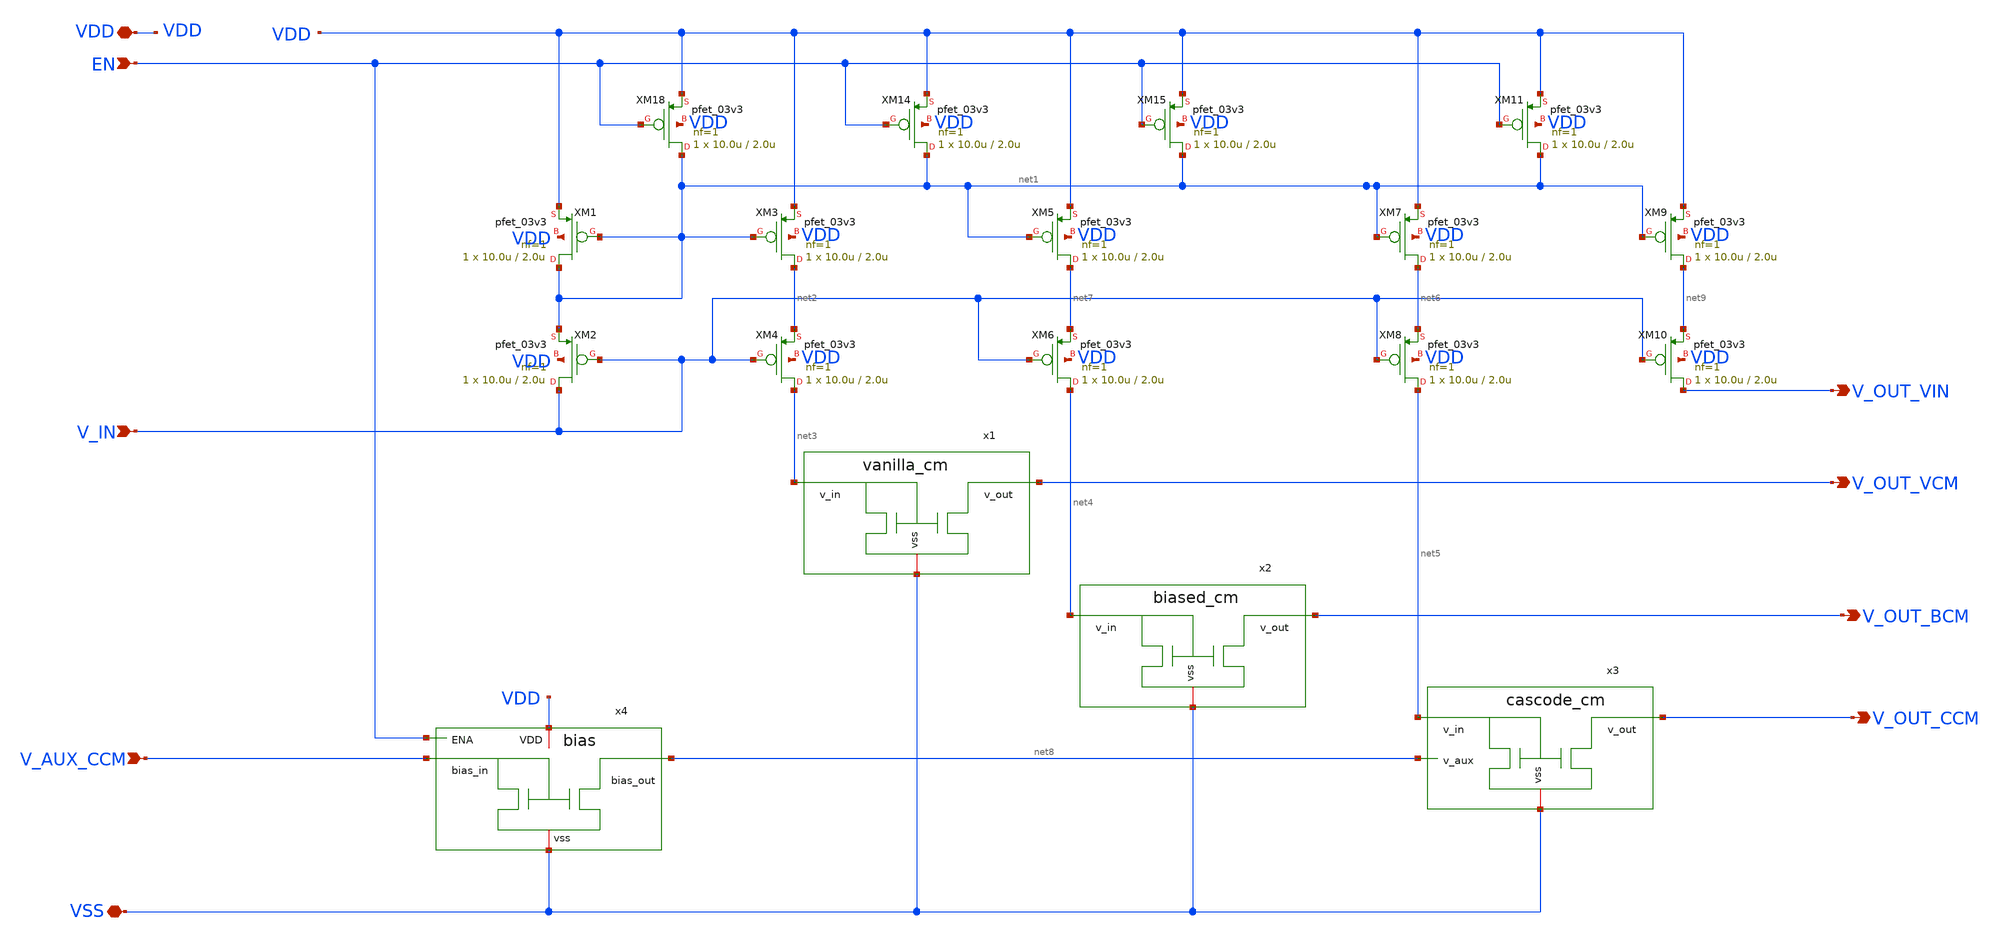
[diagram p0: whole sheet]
** sch_path: blocks/composite/regulated_cascoded_cmirror/xschem/top_level.sch
**.subckt top_level VSS V_AUX_CCM VDD V_OUT_VCM V_OUT_BCM V_OUT_CCM V_IN EN V_OUT_VIN
*.iopin VSS
*.ipin V_AUX_CCM
*.iopin VDD
*.opin V_OUT_VCM
*.opin V_OUT_BCM
*.opin V_OUT_CCM
*.ipin V_IN
*.ipin EN
*.opin V_OUT_VIN
XM1 net1 net1 VDD VDD pfet_03v3 L=2.0u W=10.0u nf=1 ad='int((nf+1)/2) * W/nf * 0.18u' as='int((nf+2)/2) * W/nf * 0.18u'
+ pd='2*int((nf+1)/2) * (W/nf + 0.18u)' ps='2*int((nf+2)/2) * (W/nf + 0.18u)' nrd='0.18u / W' nrs='0.18u / W'
+ sa=0 sb=0 sd=0 m=1
XM2 V_IN V_IN net1 VDD pfet_03v3 L=2.0u W=10.0u nf=1 ad='int((nf+1)/2) * W/nf * 0.18u' as='int((nf+2)/2) * W/nf * 0.18u'
+ pd='2*int((nf+1)/2) * (W/nf + 0.18u)' ps='2*int((nf+2)/2) * (W/nf + 0.18u)' nrd='0.18u / W' nrs='0.18u / W'
+ sa=0 sb=0 sd=0 m=1
XM3 net2 net1 VDD VDD pfet_03v3 L=2.0u W=10.0u nf=1 ad='int((nf+1)/2) * W/nf * 0.18u' as='int((nf+2)/2) * W/nf * 0.18u'
+ pd='2*int((nf+1)/2) * (W/nf + 0.18u)' ps='2*int((nf+2)/2) * (W/nf + 0.18u)' nrd='0.18u / W' nrs='0.18u / W'
+ sa=0 sb=0 sd=0 m=1
XM4 net3 V_IN net2 VDD pfet_03v3 L=2.0u W=10.0u nf=1 ad='int((nf+1)/2) * W/nf * 0.18u' as='int((nf+2)/2) * W/nf * 0.18u'
+ pd='2*int((nf+1)/2) * (W/nf + 0.18u)' ps='2*int((nf+2)/2) * (W/nf + 0.18u)' nrd='0.18u / W' nrs='0.18u / W'
+ sa=0 sb=0 sd=0 m=1
XM5 net7 net1 VDD VDD pfet_03v3 L=2.0u W=10.0u nf=1 ad='int((nf+1)/2) * W/nf * 0.18u' as='int((nf+2)/2) * W/nf * 0.18u'
+ pd='2*int((nf+1)/2) * (W/nf + 0.18u)' ps='2*int((nf+2)/2) * (W/nf + 0.18u)' nrd='0.18u / W' nrs='0.18u / W'
+ sa=0 sb=0 sd=0 m=1
XM6 net4 V_IN net7 VDD pfet_03v3 L=2.0u W=10.0u nf=1 ad='int((nf+1)/2) * W/nf * 0.18u' as='int((nf+2)/2) * W/nf * 0.18u'
+ pd='2*int((nf+1)/2) * (W/nf + 0.18u)' ps='2*int((nf+2)/2) * (W/nf + 0.18u)' nrd='0.18u / W' nrs='0.18u / W'
+ sa=0 sb=0 sd=0 m=1
XM7 net6 net1 VDD VDD pfet_03v3 L=2.0u W=10.0u nf=1 ad='int((nf+1)/2) * W/nf * 0.18u' as='int((nf+2)/2) * W/nf * 0.18u'
+ pd='2*int((nf+1)/2) * (W/nf + 0.18u)' ps='2*int((nf+2)/2) * (W/nf + 0.18u)' nrd='0.18u / W' nrs='0.18u / W'
+ sa=0 sb=0 sd=0 m=1
XM8 net5 V_IN net6 VDD pfet_03v3 L=2.0u W=10.0u nf=1 ad='int((nf+1)/2) * W/nf * 0.18u' as='int((nf+2)/2) * W/nf * 0.18u'
+ pd='2*int((nf+1)/2) * (W/nf + 0.18u)' ps='2*int((nf+2)/2) * (W/nf + 0.18u)' nrd='0.18u / W' nrs='0.18u / W'
+ sa=0 sb=0 sd=0 m=1
XM14 net1 EN VDD VDD pfet_03v3 L=2.0u W=10.0u nf=1 ad='int((nf+1)/2) * W/nf * 0.18u' as='int((nf+2)/2) * W/nf * 0.18u'
+ pd='2*int((nf+1)/2) * (W/nf + 0.18u)' ps='2*int((nf+2)/2) * (W/nf + 0.18u)' nrd='0.18u / W' nrs='0.18u / W'
+ sa=0 sb=0 sd=0 m=1
XM18 net1 EN VDD VDD pfet_03v3 L=2.0u W=10.0u nf=1 ad='int((nf+1)/2) * W/nf * 0.18u' as='int((nf+2)/2) * W/nf * 0.18u'
+ pd='2*int((nf+1)/2) * (W/nf + 0.18u)' ps='2*int((nf+2)/2) * (W/nf + 0.18u)' nrd='0.18u / W' nrs='0.18u / W'
+ sa=0 sb=0 sd=0 m=1
XM15 net1 EN VDD VDD pfet_03v3 L=2.0u W=10.0u nf=1 ad='int((nf+1)/2) * W/nf * 0.18u' as='int((nf+2)/2) * W/nf * 0.18u'
+ pd='2*int((nf+1)/2) * (W/nf + 0.18u)' ps='2*int((nf+2)/2) * (W/nf + 0.18u)' nrd='0.18u / W' nrs='0.18u / W'
+ sa=0 sb=0 sd=0 m=1
x1 net3 V_OUT_VCM VSS vanilla_cm
x2 V_OUT_BCM net4 VSS biased_cm
x3 V_OUT_CCM net8 net5 VSS cascode_cm
x4 VDD EN V_AUX_CCM net8 VSS bias
XM9 net9 net1 VDD VDD pfet_03v3 L=2.0u W=10.0u nf=1 ad='int((nf+1)/2) * W/nf * 0.18u' as='int((nf+2)/2) * W/nf * 0.18u'
+ pd='2*int((nf+1)/2) * (W/nf + 0.18u)' ps='2*int((nf+2)/2) * (W/nf + 0.18u)' nrd='0.18u / W' nrs='0.18u / W'
+ sa=0 sb=0 sd=0 m=1
XM10 V_OUT_VIN V_IN net9 VDD pfet_03v3 L=2.0u W=10.0u nf=1 ad='int((nf+1)/2) * W/nf * 0.18u' as='int((nf+2)/2) * W/nf * 0.18u'
+ pd='2*int((nf+1)/2) * (W/nf + 0.18u)' ps='2*int((nf+2)/2) * (W/nf + 0.18u)' nrd='0.18u / W' nrs='0.18u / W'
+ sa=0 sb=0 sd=0 m=1
XM11 net1 EN VDD VDD pfet_03v3 L=2.0u W=10.0u nf=1 ad='int((nf+1)/2) * W/nf * 0.18u' as='int((nf+2)/2) * W/nf * 0.18u'
+ pd='2*int((nf+1)/2) * (W/nf + 0.18u)' ps='2*int((nf+2)/2) * (W/nf + 0.18u)' nrd='0.18u / W' nrs='0.18u / W'
+ sa=0 sb=0 sd=0 m=1
**.ends

* expanding   symbol:  vanilla_cm.sym # of pins=3
** sym_path: vanilla_cm.sym
** sch_path: vanilla_cm.sch
.subckt vanilla_cm v_in v_out vss
*.ipin v_in
*.iopin vss
*.opin v_out
XM1 v_out v_in vss vss nfet_03v3 L=1u W=4u nf=1 ad='int((nf+1)/2) * W/nf * 0.18u' as='int((nf+2)/2) * W/nf * 0.18u'
+ pd='2*int((nf+1)/2) * (W/nf + 0.18u)' ps='2*int((nf+2)/2) * (W/nf + 0.18u)' nrd='0.18u / W' nrs='0.18u / W'
+ sa=0 sb=0 sd=0 m=1
XM2 v_in v_in vss vss nfet_03v3 L=1u W=4u nf=1 ad='int((nf+1)/2) * W/nf * 0.18u' as='int((nf+2)/2) * W/nf * 0.18u'
+ pd='2*int((nf+1)/2) * (W/nf + 0.18u)' ps='2*int((nf+2)/2) * (W/nf + 0.18u)' nrd='0.18u / W' nrs='0.18u / W'
+ sa=0 sb=0 sd=0 m=1
.ends


* expanding   symbol:  biased_cm.sym # of pins=3
** sym_path: biased_cm.sym
** sch_path: biased_cm.sch
.subckt biased_cm v_out v_in vss
*.ipin v_in
*.iopin vss
*.opin v_out
XM3 net2 net1 vss vss nfet_03v3 L=1u W=4u nf=1 ad='int((nf+1)/2) * W/nf * 0.18u' as='int((nf+2)/2) * W/nf * 0.18u'
+ pd='2*int((nf+1)/2) * (W/nf + 0.18u)' ps='2*int((nf+2)/2) * (W/nf + 0.18u)' nrd='0.18u / W' nrs='0.18u / W'
+ sa=0 sb=0 sd=0 m=1
XM4 net1 net1 vss vss nfet_03v3 L=1u W=4u nf=1 ad='int((nf+1)/2) * W/nf * 0.18u' as='int((nf+2)/2) * W/nf * 0.18u'
+ pd='2*int((nf+1)/2) * (W/nf + 0.18u)' ps='2*int((nf+2)/2) * (W/nf + 0.18u)' nrd='0.18u / W' nrs='0.18u / W'
+ sa=0 sb=0 sd=0 m=1
XM5 v_out v_in net2 vss nfet_03v3 L=1u W=4u nf=1 ad='int((nf+1)/2) * W/nf * 0.18u' as='int((nf+2)/2) * W/nf * 0.18u'
+ pd='2*int((nf+1)/2) * (W/nf + 0.18u)' ps='2*int((nf+2)/2) * (W/nf + 0.18u)' nrd='0.18u / W' nrs='0.18u / W'
+ sa=0 sb=0 sd=0 m=1
XM6 v_in v_in net1 vss nfet_03v3 L=1u W=4u nf=1 ad='int((nf+1)/2) * W/nf * 0.18u' as='int((nf+2)/2) * W/nf * 0.18u'
+ pd='2*int((nf+1)/2) * (W/nf + 0.18u)' ps='2*int((nf+2)/2) * (W/nf + 0.18u)' nrd='0.18u / W' nrs='0.18u / W'
+ sa=0 sb=0 sd=0 m=1
.ends


* expanding   symbol:  cascode_cm.sym # of pins=4
** sym_path: cascode_cm.sym
** sch_path: cascode_cm.sch
.subckt cascode_cm v_out v_aux v_in vss
*.ipin v_in
*.iopin vss
*.ipin v_aux
*.opin v_out
XM10 v_aux net1 vss vss nfet_03v3 L=1u W=5u nf=1 ad='int((nf+1)/2) * W/nf * 0.18u' as='int((nf+2)/2) * W/nf * 0.18u'
+ pd='2*int((nf+1)/2) * (W/nf + 0.18u)' ps='2*int((nf+2)/2) * (W/nf + 0.18u)' nrd='0.18u / W' nrs='0.18u / W'
+ sa=0 sb=0 sd=0 m=1
XM8 v_in v_aux net1 vss nfet_03v3 L=1u W=5u nf=1 ad='int((nf+1)/2) * W/nf * 0.18u' as='int((nf+2)/2) * W/nf * 0.18u'
+ pd='2*int((nf+1)/2) * (W/nf + 0.18u)' ps='2*int((nf+2)/2) * (W/nf + 0.18u)' nrd='0.18u / W' nrs='0.18u / W'
+ sa=0 sb=0 sd=0 m=1
XM11 net1 v_in vss vss nfet_03v3 L=1u W=5u nf=1 ad='int((nf+1)/2) * W/nf * 0.18u' as='int((nf+2)/2) * W/nf * 0.18u'
+ pd='2*int((nf+1)/2) * (W/nf + 0.18u)' ps='2*int((nf+2)/2) * (W/nf + 0.18u)' nrd='0.18u / W' nrs='0.18u / W'
+ sa=0 sb=0 sd=0 m=1
XM12 v_aux net2 vss vss nfet_03v3 L=1u W=5u nf=1 ad='int((nf+1)/2) * W/nf * 0.18u' as='int((nf+2)/2) * W/nf * 0.18u'
+ pd='2*int((nf+1)/2) * (W/nf + 0.18u)' ps='2*int((nf+2)/2) * (W/nf + 0.18u)' nrd='0.18u / W' nrs='0.18u / W'
+ sa=0 sb=0 sd=0 m=1
XM13 net2 v_in vss vss nfet_03v3 L=1u W=5u nf=1 ad='int((nf+1)/2) * W/nf * 0.18u' as='int((nf+2)/2) * W/nf * 0.18u'
+ pd='2*int((nf+1)/2) * (W/nf + 0.18u)' ps='2*int((nf+2)/2) * (W/nf + 0.18u)' nrd='0.18u / W' nrs='0.18u / W'
+ sa=0 sb=0 sd=0 m=1
XM14 v_out v_aux net2 vss nfet_03v3 L=1u W=5u nf=1 ad='int((nf+1)/2) * W/nf * 0.18u' as='int((nf+2)/2) * W/nf * 0.18u'
+ pd='2*int((nf+1)/2) * (W/nf + 0.18u)' ps='2*int((nf+2)/2) * (W/nf + 0.18u)' nrd='0.18u / W' nrs='0.18u / W'
+ sa=0 sb=0 sd=0 m=1
.ends


* expanding   symbol:  bias.sym # of pins=5
** sym_path: bias.sym
** sch_path: bias.sch
.subckt bias VDD ENA bias_in bias_out vss
*.iopin vss
*.iopin VDD
*.ipin ENA
*.ipin bias_in
*.opin bias_out
XM11 net1 net1 VDD VDD pfet_03v3 L=2.0u W=100.0u nf=10 ad='int((nf+1)/2) * W/nf * 0.18u' as='int((nf+2)/2) * W/nf * 0.18u'
+ pd='2*int((nf+1)/2) * (W/nf + 0.18u)' ps='2*int((nf+2)/2) * (W/nf + 0.18u)' nrd='0.18u / W' nrs='0.18u / W'
+ sa=0 sb=0 sd=0 m=1
XM12 bias_in bias_in net1 VDD pfet_03v3 L=2.0u W=100.0u nf=10 ad='int((nf+1)/2) * W/nf * 0.18u' as='int((nf+2)/2) * W/nf * 0.18u'
+ pd='2*int((nf+1)/2) * (W/nf + 0.18u)' ps='2*int((nf+2)/2) * (W/nf + 0.18u)' nrd='0.18u / W' nrs='0.18u / W'
+ sa=0 sb=0 sd=0 m=1
XM16 net1 ENA VDD VDD pfet_03v3 L=2.0u W=10.0u nf=1 ad='int((nf+1)/2) * W/nf * 0.18u' as='int((nf+2)/2) * W/nf * 0.18u'
+ pd='2*int((nf+1)/2) * (W/nf + 0.18u)' ps='2*int((nf+2)/2) * (W/nf + 0.18u)' nrd='0.18u / W' nrs='0.18u / W'
+ sa=0 sb=0 sd=0 m=1
XM17 net2 net1 VDD VDD pfet_03v3 L=2.0u W=10.0u nf=1 ad='int((nf+1)/2) * W/nf * 0.18u' as='int((nf+2)/2) * W/nf * 0.18u'
+ pd='2*int((nf+1)/2) * (W/nf + 0.18u)' ps='2*int((nf+2)/2) * (W/nf + 0.18u)' nrd='0.18u / W' nrs='0.18u / W'
+ sa=0 sb=0 sd=0 m=1
XM19 net3 bias_in net2 VDD pfet_03v3 L=2.0u W=10.0u nf=1 ad='int((nf+1)/2) * W/nf * 0.18u' as='int((nf+2)/2) * W/nf * 0.18u'
+ pd='2*int((nf+1)/2) * (W/nf + 0.18u)' ps='2*int((nf+2)/2) * (W/nf + 0.18u)' nrd='0.18u / W' nrs='0.18u / W'
+ sa=0 sb=0 sd=0 m=1
XM9 net4 net4 VDD VDD pfet_03v3 L=2.0u W=100.0u nf=10 ad='int((nf+1)/2) * W/nf * 0.18u' as='int((nf+2)/2) * W/nf * 0.18u'
+ pd='2*int((nf+1)/2) * (W/nf + 0.18u)' ps='2*int((nf+2)/2) * (W/nf + 0.18u)' nrd='0.18u / W' nrs='0.18u / W'
+ sa=0 sb=0 sd=0 m=1
XM10 net5 net5 net4 VDD pfet_03v3 L=2.0u W=100.0u nf=10 ad='int((nf+1)/2) * W/nf * 0.18u' as='int((nf+2)/2) * W/nf * 0.18u'
+ pd='2*int((nf+1)/2) * (W/nf + 0.18u)' ps='2*int((nf+2)/2) * (W/nf + 0.18u)' nrd='0.18u / W' nrs='0.18u / W'
+ sa=0 sb=0 sd=0 m=1
XM13 net4 ENA VDD VDD pfet_03v3 L=2.0u W=10.0u nf=1 ad='int((nf+1)/2) * W/nf * 0.18u' as='int((nf+2)/2) * W/nf * 0.18u'
+ pd='2*int((nf+1)/2) * (W/nf + 0.18u)' ps='2*int((nf+2)/2) * (W/nf + 0.18u)' nrd='0.18u / W' nrs='0.18u / W'
+ sa=0 sb=0 sd=0 m=1
XM20 net6 net4 VDD VDD pfet_03v3 L=2.0u W=10.0u nf=1 ad='int((nf+1)/2) * W/nf * 0.18u' as='int((nf+2)/2) * W/nf * 0.18u'
+ pd='2*int((nf+1)/2) * (W/nf + 0.18u)' ps='2*int((nf+2)/2) * (W/nf + 0.18u)' nrd='0.18u / W' nrs='0.18u / W'
+ sa=0 sb=0 sd=0 m=1
XM21 bias_out net5 net6 VDD pfet_03v3 L=2.0u W=10.0u nf=10 ad='int((nf+1)/2) * W/nf * 0.18u' as='int((nf+2)/2) * W/nf * 0.18u'
+ pd='2*int((nf+1)/2) * (W/nf + 0.18u)' ps='2*int((nf+2)/2) * (W/nf + 0.18u)' nrd='0.18u / W' nrs='0.18u / W'
+ sa=0 sb=0 sd=0 m=1
XM22 net8 net7 vss vss nfet_03v3 L=1u W=8u nf=1 ad='int((nf+1)/2) * W/nf * 0.18u' as='int((nf+2)/2) * W/nf * 0.18u'
+ pd='2*int((nf+1)/2) * (W/nf + 0.18u)' ps='2*int((nf+2)/2) * (W/nf + 0.18u)' nrd='0.18u / W' nrs='0.18u / W'
+ sa=0 sb=0 sd=0 m=1
XM23 net7 net7 vss vss nfet_03v3 L=1u W=80u nf=10 ad='int((nf+1)/2) * W/nf * 0.18u' as='int((nf+2)/2) * W/nf * 0.18u'
+ pd='2*int((nf+1)/2) * (W/nf + 0.18u)' ps='2*int((nf+2)/2) * (W/nf + 0.18u)' nrd='0.18u / W' nrs='0.18u / W'
+ sa=0 sb=0 sd=0 m=1
XM24 net5 net3 net8 vss nfet_03v3 L=1u W=8u nf=1 ad='int((nf+1)/2) * W/nf * 0.18u' as='int((nf+2)/2) * W/nf * 0.18u'
+ pd='2*int((nf+1)/2) * (W/nf + 0.18u)' ps='2*int((nf+2)/2) * (W/nf + 0.18u)' nrd='0.18u / W' nrs='0.18u / W'
+ sa=0 sb=0 sd=0 m=1
XM25 net3 net3 net7 vss nfet_03v3 L=1u W=80u nf=10 ad='int((nf+1)/2) * W/nf * 0.18u' as='int((nf+2)/2) * W/nf * 0.18u'
+ pd='2*int((nf+1)/2) * (W/nf + 0.18u)' ps='2*int((nf+2)/2) * (W/nf + 0.18u)' nrd='0.18u / W' nrs='0.18u / W'
+ sa=0 sb=0 sd=0 m=1
.ends

.end
